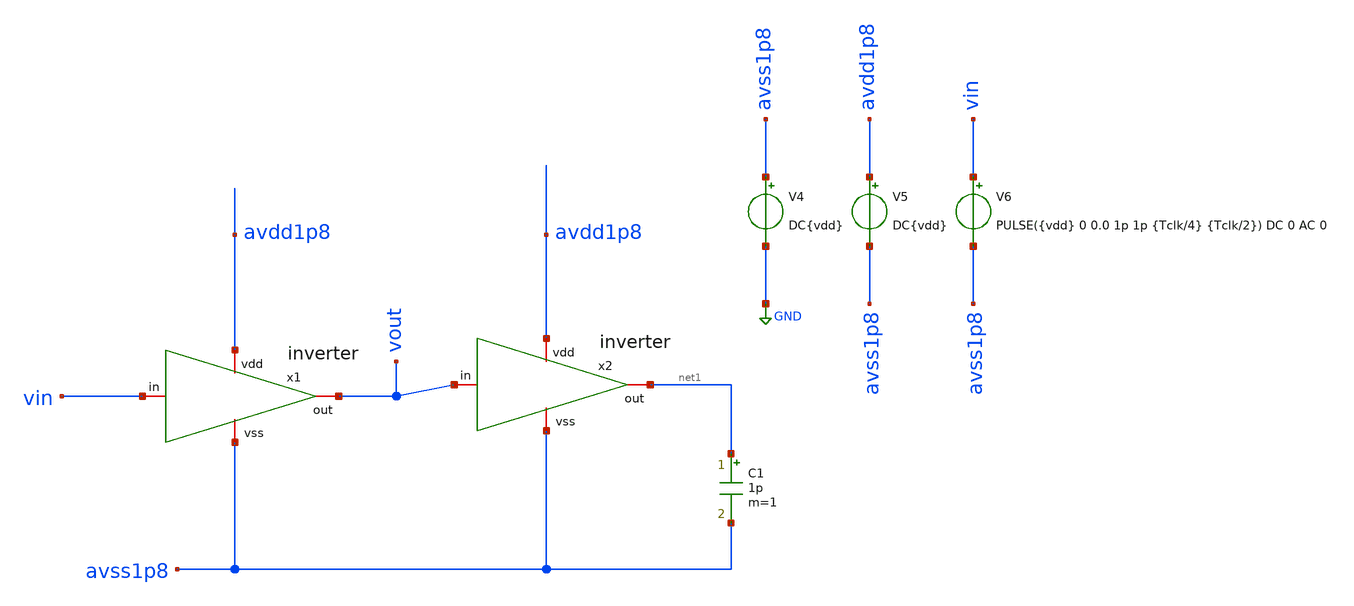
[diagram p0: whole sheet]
** sch_path: verification/testbenches/inverter/tb_inverter.sch
**.subckt tb_inverter
C1 net1 avss1p8 1p m=1
V4 avss1p8 GND DC{vdd}
V5 avdd1p8 avss1p8 DC{vdd}
V6 vin avss1p8 PULSE({vdd} 0 0.0 1p 1p {Tclk/4} {Tclk/2}) DC 0 AC 0
x1 avdd1p8 vin vout avss1p8 inverter
x2 avdd1p8 vout net1 avss1p8 inverter
**** begin user architecture code


* Circuit Parameters
.param vdd = 1.2
.param vss = 0.0
.param Tclk = 10n
.options TEMP = 27.0
* Include Models - IHP SG13G2
.lib cornerMOSlv.lib mos_tt
* OP Parameters & Singals to save
.save all
*Simulations
.control
tran 0.01u 100n
setplot tran1
plot v(vin) v(vout)+1.2
reset
dc V6 0 1.2 0.01
setplot dc
plot vin vout ylabel vout xlabel vin
set filetype = ascii
write dcsweep.raw
.endc
.end


**** end user architecture code
**.ends

* expanding   symbol:  blocks/inverter/schematic/inverter.sym # of pins=4
** sym_path: design/blocks/inverter/schematic/inverter.sym
** sch_path: design/blocks/inverter/schematic/inverter.sch
.subckt inverter vdd in out vss
*.iopin in
*.iopin out
*.iopin vss
*.iopin vdd
XM1 out in vdd vdd sg13_lv_pmos w=0.15u l=0.13u ng=1 m=1 mm_ok=1
XM2 out in vss vss sg13_lv_nmos w=0.15u l=0.13u ng=1 m=1 mm_ok=1
.ends

.GLOBAL GND
.end
